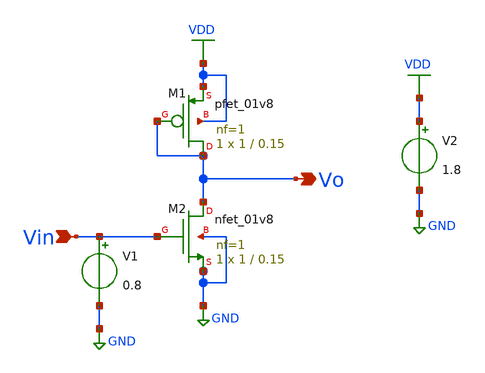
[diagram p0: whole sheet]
** sch_path: SINGLE_STAGE_AMP/CS_DIODE/cs_diode.sch
**.subckt cs_diode Vo Vin
*.opin Vo
*.ipin Vin
XM1 Vo Vo VDD VDD sky130_fd_pr__pfet_01v8 L=0.15 W=1 nf=1 ad='int((1 + 1)/2) * 1 / 1 * 0.29' as='int((1 + 2)/2) * 1 / 1 * 0.29'
+ pd='2*int((1 + 1)/2) * (1 / 1 + 0.29)' ps='2*int((1 + 2)/2) * (1 / 1 + 0.29)' nrd='0.29 / 1 ' nrs='0.29 / 1 '
+ sa=0 sb=0 sd=0 mult=1 m=1
XM2 Vo Vin GND GND sky130_fd_pr__nfet_01v8 L=0.15 W=1 nf=1 ad='int((1 + 1)/2) * 1 / 1 * 0.29' as='int((1 + 2)/2) * 1 / 1 * 0.29'
+ pd='2*int((1 + 1)/2) * (1 / 1 + 0.29)' ps='2*int((1 + 2)/2) * (1 / 1 + 0.29)' nrd='0.29 / 1 ' nrs='0.29 / 1 '
+ sa=0 sb=0 sd=0 mult=1 m=1
V1 Vin GND 0.8
V2 VDD GND 1.8
**.ends
.GLOBAL VDD
.GLOBAL GND
.end
